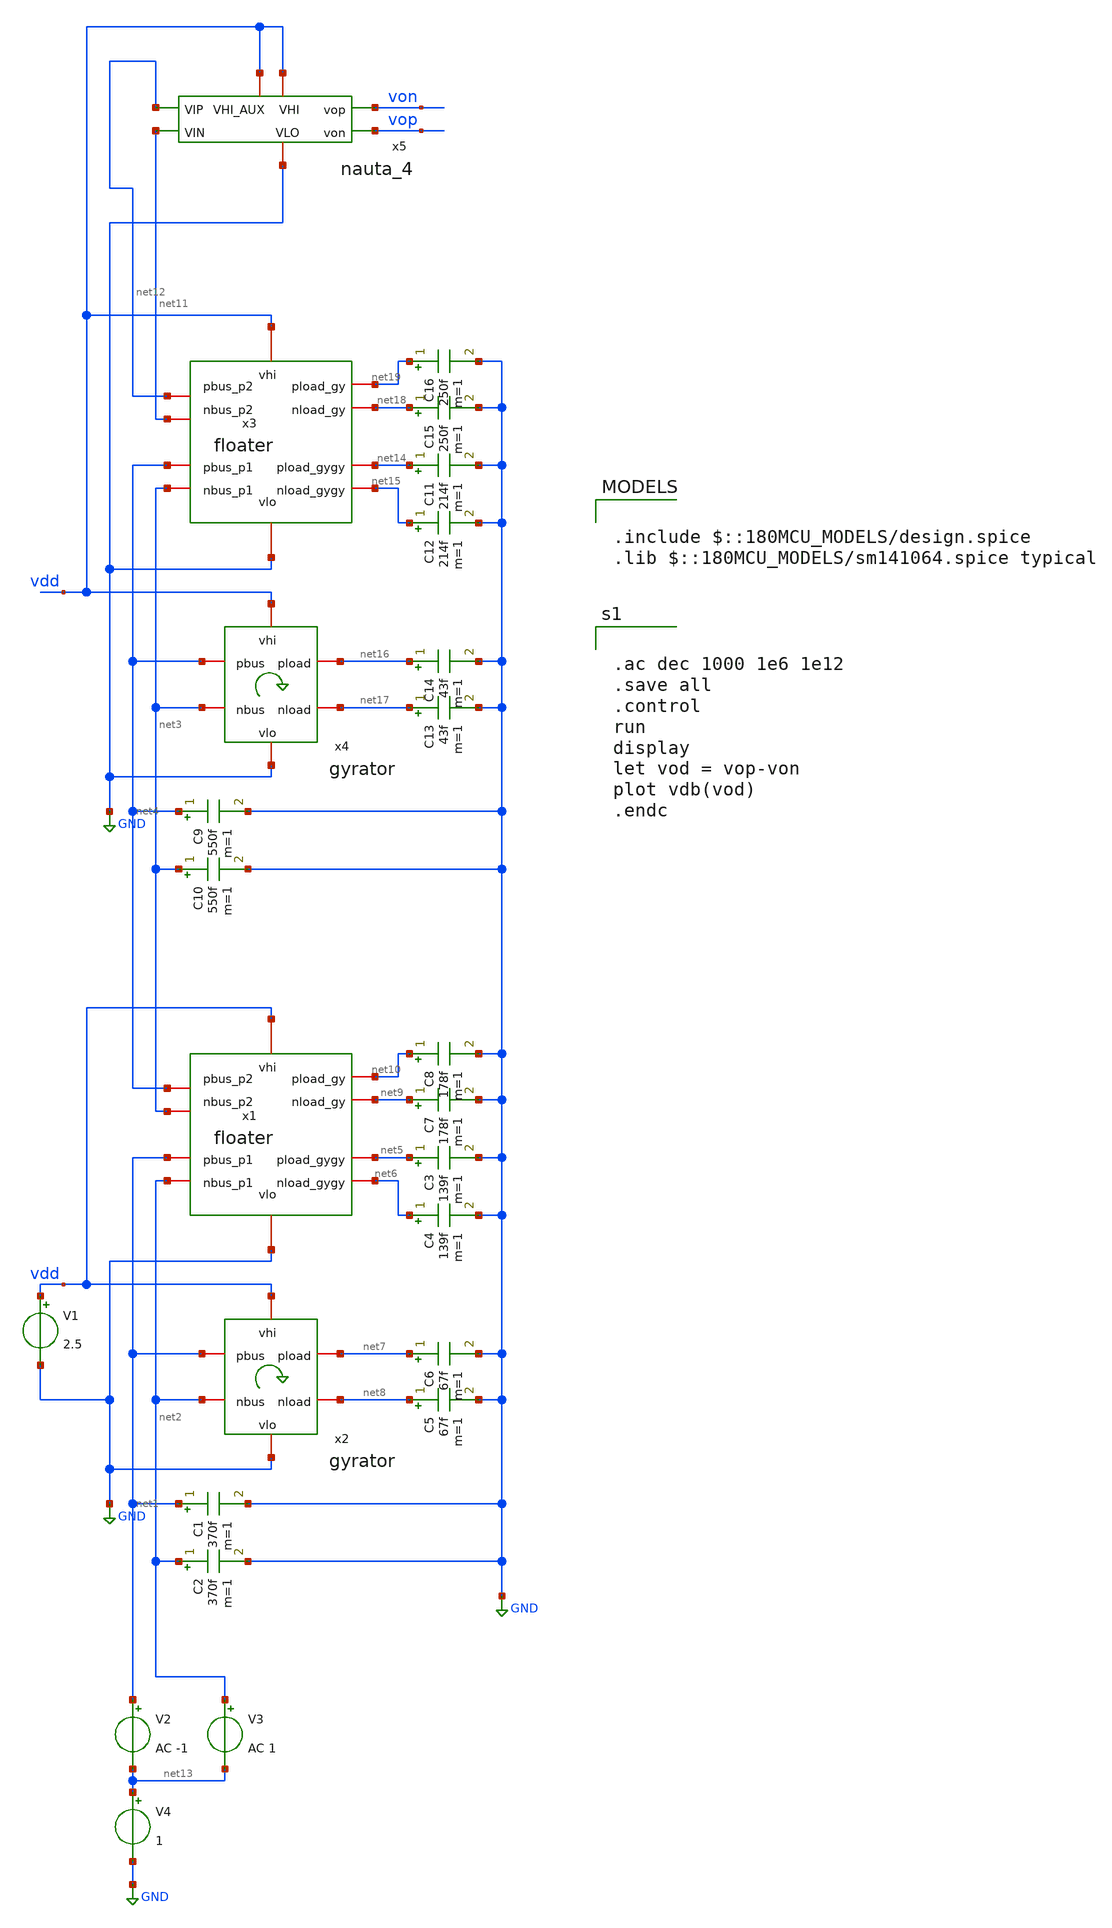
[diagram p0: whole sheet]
** sch_path: xschem/chebyshev_test.sch
**.subckt chebyshev_test
x1 vdd net4 net3 net9 net10 GND net6 net5 net1 net2 floater
x2 vdd net7 net1 net8 net2 GND gyrator
C1 net1 GND 370f m=1
C2 net2 GND 370f m=1
C3 net5 GND 139f m=1
C4 net6 GND 139f m=1
C5 net8 GND 67f m=1
C6 net7 GND 67f m=1
C7 net9 GND 178f m=1
C8 net10 GND 178f m=1
V1 vdd GND 2.5
V2 net1 net13 AC -1
V3 net2 net13 AC 1
V4 net13 GND 1
x3 vdd net12 net11 net18 net19 GND net15 net14 net4 net3 floater
x4 vdd net16 net4 net17 net3 GND gyrator
C9 net4 GND 550f m=1
C10 net3 GND 550f m=1
C11 net14 GND 214f m=1
C12 net15 GND 214f m=1
C13 net17 GND 43f m=1
C14 net16 GND 43f m=1
C15 net18 GND 250f m=1
C16 net19 GND 250f m=1
x5 vdd vdd net12 von net11 vop GND nauta_4
**** begin user architecture code


.ac dec 1000 1e6 1e12
.save all
.control
run
display
let vod = vop-von
plot vdb(vod)
.endc



.include $::180MCU_MODELS/design.spice
.lib $::180MCU_MODELS/sm141064.spice typical

**** end user architecture code
**.ends

* expanding   symbol:  floater.sym # of pins=10
** sym_path: xschem/floater.sym
** sch_path: xschem/floater.sch
.subckt floater vhi pbus_p2 nbus_p2 nload_gy pload_gy vlo nload_gygy pload_gygy pbus_p1 nbus_p1
*.iopin nbus_p1
*.iopin pbus_p1
*.iopin nbus_p2
*.iopin pbus_p2
*.iopin vhi
*.iopin vlo
*.iopin pload_gy
*.iopin nload_gy
*.iopin pload_gygy
*.iopin nload_gygy
x1 vhi vhi nbus_p2 pload_gy pbus_p2 nload_gy vlo nauta_4
x2 vhi vhi nload_gy nbus_p2 pload_gy nbus_p1 vlo nauta_4
x3 vhi vhi pload_gy pbus_p2 nload_gy pbus_p1 vlo nauta_4
x4 vhi vhi nbus_p1 nload_gy pbus_p1 pload_gy vlo nauta_4
x5 vhi nload_gygy nload_gy pload_gygy pload_gy vlo gyrator
x6 vhi vhi nbus_p2 pload_gy pbus_p2 nload_gy vlo nauta_4
x7 vhi vhi nbus_p2 pload_gy pbus_p2 nload_gy vlo nauta_4
x8 vhi vhi nbus_p2 pload_gy pbus_p2 nload_gy vlo nauta_4
x9 vhi vhi nbus_p2 pload_gy pbus_p2 nload_gy vlo nauta_4
x10 vhi vhi nload_gy nbus_p2 pload_gy nbus_p1 vlo nauta_4
x11 vhi vhi nload_gy nbus_p2 pload_gy nbus_p1 vlo nauta_4
x12 vhi vhi nload_gy nbus_p2 pload_gy nbus_p1 vlo nauta_4
x13 vhi vhi nload_gy nbus_p2 pload_gy nbus_p1 vlo nauta_4
x14 vhi vhi pload_gy pbus_p2 nload_gy pbus_p1 vlo nauta_4
x15 vhi vhi pload_gy pbus_p2 nload_gy pbus_p1 vlo nauta_4
x16 vhi vhi pload_gy pbus_p2 nload_gy pbus_p1 vlo nauta_4
x17 vhi vhi pload_gy pbus_p2 nload_gy pbus_p1 vlo nauta_4
x18 vhi vhi nbus_p1 nload_gy pbus_p1 pload_gy vlo nauta_4
x19 vhi vhi nbus_p1 nload_gy pbus_p1 pload_gy vlo nauta_4
x20 vhi vhi nbus_p1 nload_gy pbus_p1 pload_gy vlo nauta_4
x21 vhi vhi nbus_p1 nload_gy pbus_p1 pload_gy vlo nauta_4
.ends


* expanding   symbol:  gyrator.sym # of pins=6
** sym_path: xschem/gyrator.sym
** sch_path: xschem/gyrator.sch
.subckt gyrator vhi pload pbus nload nbus vlo
*.iopin nbus
*.iopin pbus
*.iopin vhi
*.iopin vlo
*.iopin pload
*.iopin nload
x1 vhi vhi pbus pload nbus nload vlo nauta_4
x2 vhi vhi nload pbus pload nbus vlo nauta_4
x3 vhi vhi pbus pload nbus nload vlo nauta_4
x4 vhi vhi pbus pload nbus nload vlo nauta_4
x5 vhi vhi pbus pload nbus nload vlo nauta_4
x6 vhi vhi pbus pload nbus nload vlo nauta_4
x7 vhi vhi nload pbus pload nbus vlo nauta_4
x8 vhi vhi nload pbus pload nbus vlo nauta_4
x9 vhi vhi nload pbus pload nbus vlo nauta_4
x10 vhi vhi nload pbus pload nbus vlo nauta_4
.ends


* expanding   symbol:  nauta_4.sym # of pins=7
** sym_path: xschem/nauta_4.sym
** sch_path: xschem/nauta_4.sch
.subckt nauta_4 VHI_AUX VHI VIP vop VIN von VLO
*.ipin VIP
*.ipin VIN
*.opin vop
*.opin von
*.iopin VHI
*.iopin VHI_AUX
*.iopin VLO
**** begin user architecture code

.subckt NAUTA VOP VON VIP VIN VHI VHI_AUX VLO

XA0N VON VIP VLO VLO nmos_6p0 w=0.82u l=0.6u
XA0P VON VIP VHI VHI pmos_6p0 w=1.22u l=0.5u
XA1N VON VIP VLO VLO nmos_6p0 w=0.82u l=0.6u
XA1P VON VIP VHI VHI pmos_6p0 w=1.22u l=0.5u

XB0N VOP VIN VLO VLO nmos_6p0 w=0.82u l=0.6u
XB0P VOP VIN VHI VHI pmos_6p0 w=1.22u l=0.5u
XB1N VOP VIN VLO VLO nmos_6p0 w=0.82u l=0.6u
XB1P VOP VIN VHI VHI pmos_6p0 w=1.22u l=0.5u

XC0N VOP VON VLO VLO nmos_6p0 w=0.82u l=0.6u
XC0P VOP VON VHI VHI pmos_6p0 w=1.22u l=0.5u

XD0N VON VOP VLO VLO nmos_6p0 w=0.82u l=0.6u
XD0P VON VOP VHI VHI pmos_6p0 w=1.22u l=0.5u

XC1N VOP VOP VLO VLO nmos_6p0 w=0.82u l=0.6u
XC1P VOP VOP VHI_AUX VHI_AUX pmos_6p0 w=1.22u l=0.5u

XD1N VON VON VLO VLO nmos_6p0 w=0.82u l=0.6u
XD1P VON VON VHI_AUX VHI_AUX pmos_6p0 w=1.22u l=0.5u

.ends

XDUT VOP VON VIP VIN VHI VHI_AUX VLO NAUTA


**** end user architecture code
.ends

.GLOBAL GND
.end
